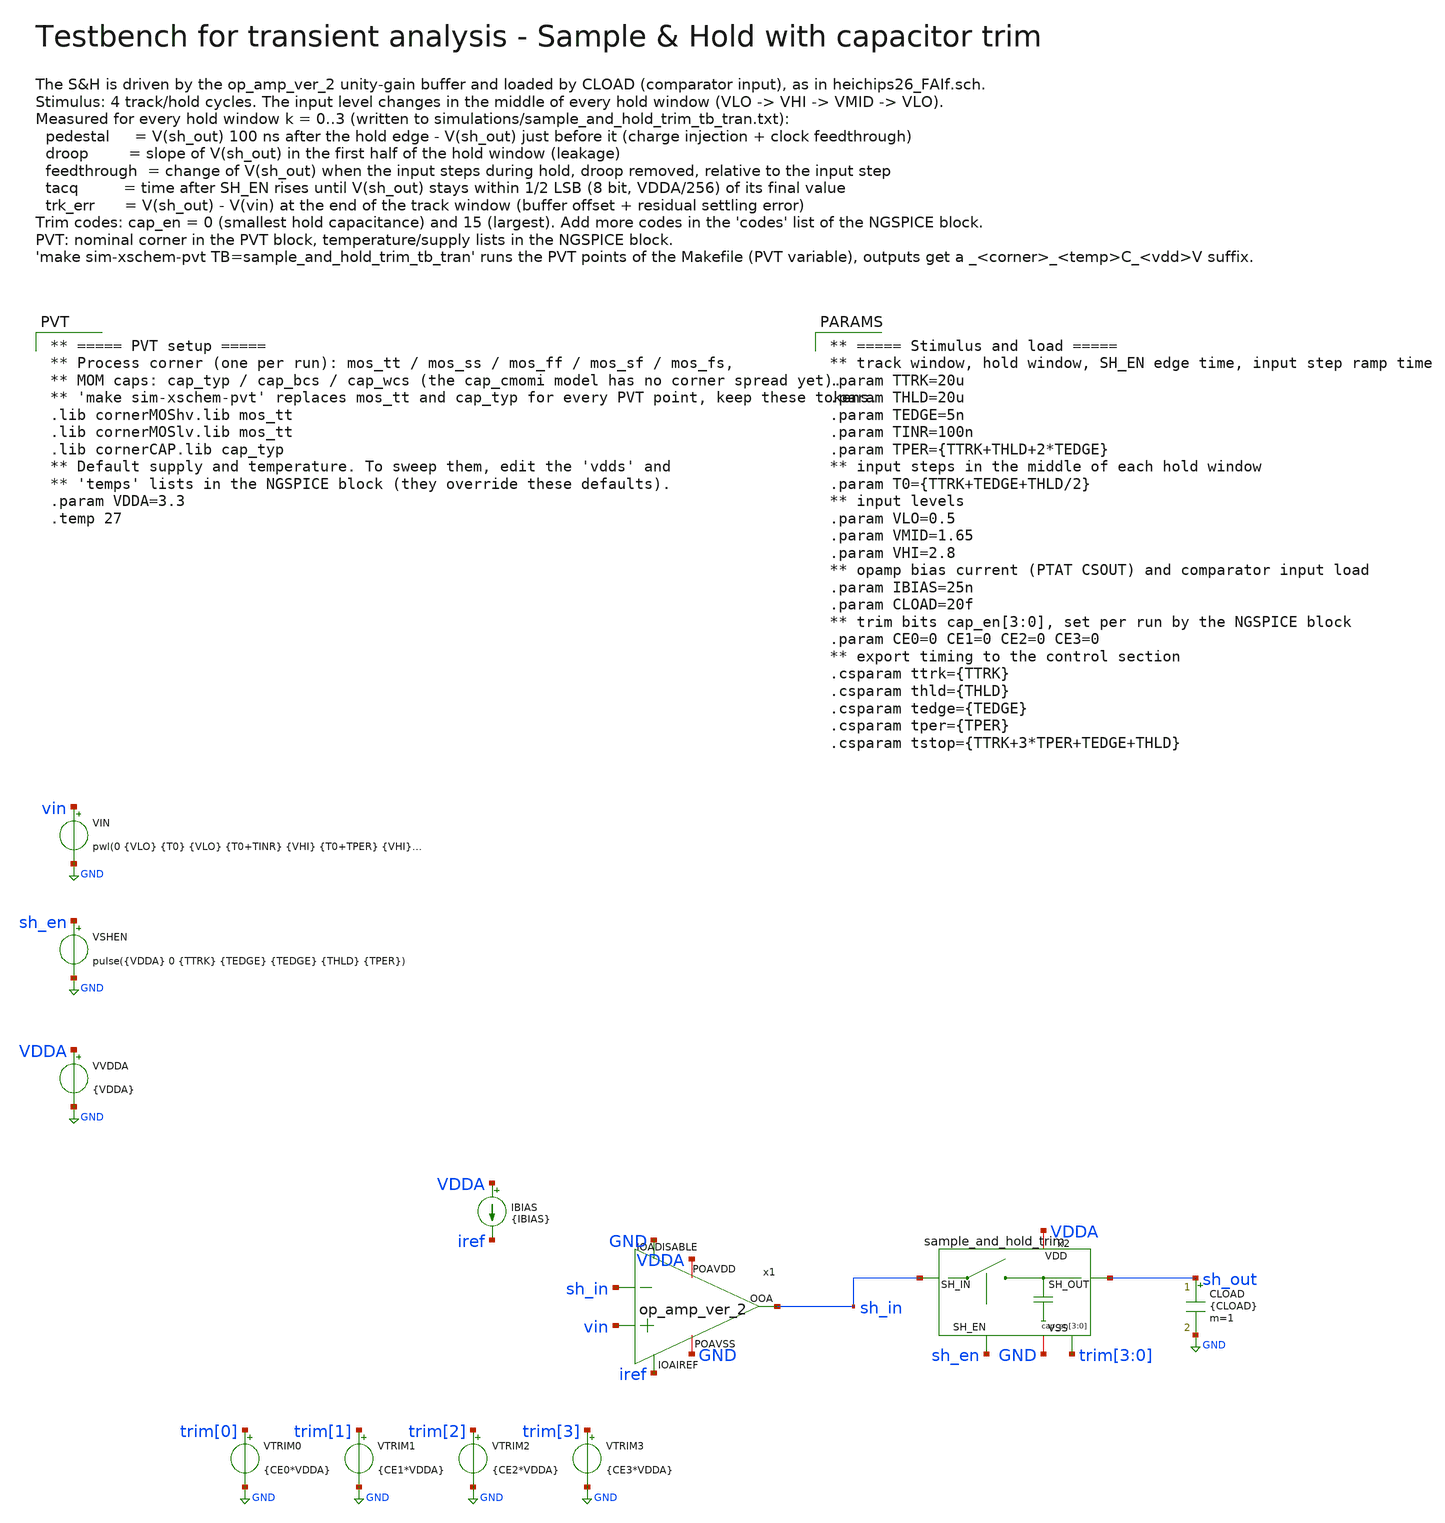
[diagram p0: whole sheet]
** sch_path: macros/heichips26_FAIf/macros/sample_and_hold_trim/testbenches/xschem/sample_and_hold_trim_tb_tran.sch
**.subckt sample_and_hold_trim_tb_tran
VVDDA VDDA GND {VDDA}
.save i(vvdda)
VIN vin GND pwl(0 {VLO} {T0} {VLO} {T0+TINR} {VHI} {T0+TPER} {VHI} {T0+TPER+TINR} {VMID} {T0+2*TPER}
+ {VMID} {T0+2*TPER+TINR} {VLO})
VSHEN sh_en GND pulse({VDDA} 0 {TTRK} {TEDGE} {TEDGE} {THLD} {TPER})
VTRIM0 trim[0] GND {CE0*VDDA}
VTRIM1 trim[1] GND {CE1*VDDA}
VTRIM2 trim[2] GND {CE2*VDDA}
VTRIM3 trim[3] GND {CE3*VDDA}
IBIAS VDDA iref {IBIAS}
x1 VDDA iref sh_in sh_in vin GND GND op_amp_ver_2
x2 VDDA sh_in sh_out sh_en GND trim[3] trim[2] trim[1] trim[0] sample_and_hold_trim
CLOAD sh_out GND {CLOAD} m=1
**** begin user architecture code
 ** ===== PVT setup =====
** Process corner (one per run): mos_tt / mos_ss / mos_ff / mos_sf / mos_fs,
** MOM caps: cap_typ / cap_bcs / cap_wcs (the cap_cmomi model has no corner spread yet).
** 'make sim-xschem-pvt' replaces mos_tt and cap_typ for every PVT point, keep these tokens.
.lib cornerMOShv.lib mos_tt
.lib cornerMOSlv.lib mos_tt
.lib cornerCAP.lib cap_typ
** Default supply and temperature. To sweep them, edit the 'vdds' and
** 'temps' lists in the NGSPICE block (they override these defaults).
.param VDDA=3.3
.temp 27


** ===== Stimulus and load =====
** track window, hold window, SH_EN edge time, input step ramp time
.param TTRK=20u
.param THLD=20u
.param TEDGE=5n
.param TINR=100n
.param TPER={TTRK+THLD+2*TEDGE}
** input steps in the middle of each hold window
.param T0={TTRK+TEDGE+THLD/2}
** input levels
.param VLO=0.5
.param VMID=1.65
.param VHI=2.8
** opamp bias current (PTAT CSOUT) and comparator input load
.param IBIAS=25n
.param CLOAD=20f
** trim bits cap_en[3:0], set per run by the NGSPICE block
.param CE0=0 CE1=0 CE2=0 CE3=0
** export timing to the control section
.csparam ttrk={TTRK}
.csparam thld={THLD}
.csparam tedge={TEDGE}
.csparam tper={TPER}
.csparam tstop={TTRK+3*TPER+TEDGE+THLD}




** gear: no trapezoidal ringing; small gmin: the droop comes from pA leakage currents
** (no klu: with the floating trim-cap nodes at cap_en=0 it stalls at tiny time steps)
.options method=gear reltol=1e-4 abstol=1e-15 gmin=1e-18
.control
  ** ===== sweep lists =====
  ** trim codes for cap_en[3:0]: 0 = smallest, 15 = largest hold capacitance
  set codes = ( 0 15 )
  ** temperature and supply sweep lists (process corner: see PVT block)
  set temps = ( 27 )
  set vdds = ( 3.3 )
  ** 'make sim-xschem-pvt' passes the PVT point with ngspice -D and adds a
  ** _<corner>_<temp>C_<vdd>V suffix to the output files
  if $?pvt_temp
    set temps = ( $pvt_temp )
  end
  if $?pvt_vdd
    set vdds = ( $pvt_vdd )
  end
  if $?pvt_corner
  else
    set pvt_corner = tt
  end
  set ext_txt = .txt
  set ext_raw = .raw
  ** output names: <tb><pvt_tag>.<ext>, the tag only exists for PVT runs
  if $?pvt_tag
    set outtxt = "@schname\$pvt_tag$ext_txt"
    set outraw = "@schname\$pvt_tag$ext_raw"
  else
    set outtxt = "@schname\$ext_txt"
    set outraw = "@schname\$ext_raw"
  end

  echo corner temp_C vdd_V code hold vin_V pedestal_mV droop_mV_per_ms feedthrough_dB tacq_us
+ trk_err_mV > $outtxt
  unset appendwrite
  foreach temp_c $temps
  foreach vdd $vdds
  foreach code $codes
    ** split the trim code into the cap_en bits
    let b0 = $code - 2*floor($code/2)
    let b1 = floor($code/2) - 2*floor($code/4)
    let b2 = floor($code/4) - 2*floor($code/8)
    let b3 = floor($code/8) - 2*floor($code/16)
    alterparam VDDA = $vdd
    alterparam CE0 = $&b0
    alterparam CE1 = $&b1
    alterparam CE2 = $&b2
    alterparam CE3 = $&b3
    reset
    ** set the temperature after reset (reset restores the netlist temperature)
    option temp = $temp_c
    ** top-level signals and the trim capacitor nodes inside the S&H
    save v(vin) v(sh_in) v(sh_out) v(sh_en) i(vvdda) v(x2.net2) v(x2.net3) v(x2.net4) v(x2.net5)
    tran 10n $&tstop
    write $outraw
    set appendwrite

    let tol = $vdd/256/2
    let k = 0
    while k < 4
      ** hold window k: SH_EN starts falling at th
      let th = ttrk + k*tper
      let tpre = th - 10n
      let tped = th + tedge + 100n
      let tdr = th + tedge + thld/2 - 10n
      let tend = th + tedge + thld - 10n
      meas tran vtrk find v(sh_out) at=$&tpre
      meas tran vped find v(sh_out) at=$&tped
      meas tran vdr find v(sh_out) at=$&tdr
      meas tran vend find v(sh_out) at=$&tend
      meas tran vlev find v(vin) at=$&tpre
      meas tran vin_dr find v(sh_in) at=$&tdr
      meas tran vin_end find v(sh_in) at=$&tend
      let ped_mv = (vped - vtrk)*1e3
      let droop = (vdr - vped)/(tdr - tped)
      let droop_mv_ms = droop
      if k < 3
        ** feedthrough of the input step during hold, droop removed
        let dvin = vin_end - vin_dr
        let dvout = (vend - vdr) - droop*(tend - tdr)
        let ft_db = db(abs(dvout/dvin) + 1e-12)
        ** acquisition of the new level in the following track window
        let ta = th + tedge + thld
        let tfin = th + tper - 10n
        meas tran vfin find v(sh_out) at=$&tfin
        meas tran vin_fin find v(vin) at=$&tfin
        let err = abs(v(sh_out) - vfin)
        meas tran errmax max err from=$&ta to=$&tfin
        if errmax > tol
          meas tran tsettled when err=$&tol fall=last from=$&ta to=$&tfin
          let tacq_us = (tsettled - ta)*1e6
        else
          let tacq_us = 0
        end
        let trk_mv = (vfin - vin_fin)*1e3
        echo $pvt_corner $temp_c $vdd $code $&k $&vlev $&ped_mv $&droop_mv_ms $&ft_db $&tacq_us
+ $&trk_mv >> $outtxt
      else
        echo $pvt_corner $temp_c $vdd $code $&k $&vlev $&ped_mv $&droop_mv_ms - - - >> $outtxt
      end
      let k = k + 1
    end
  end
  end
  end
  echo
  echo ===== Results: simulations/$outtxt =====
  shell cat $outtxt
.endc


**** end user architecture code
**.ends
.GLOBAL GND
.end
